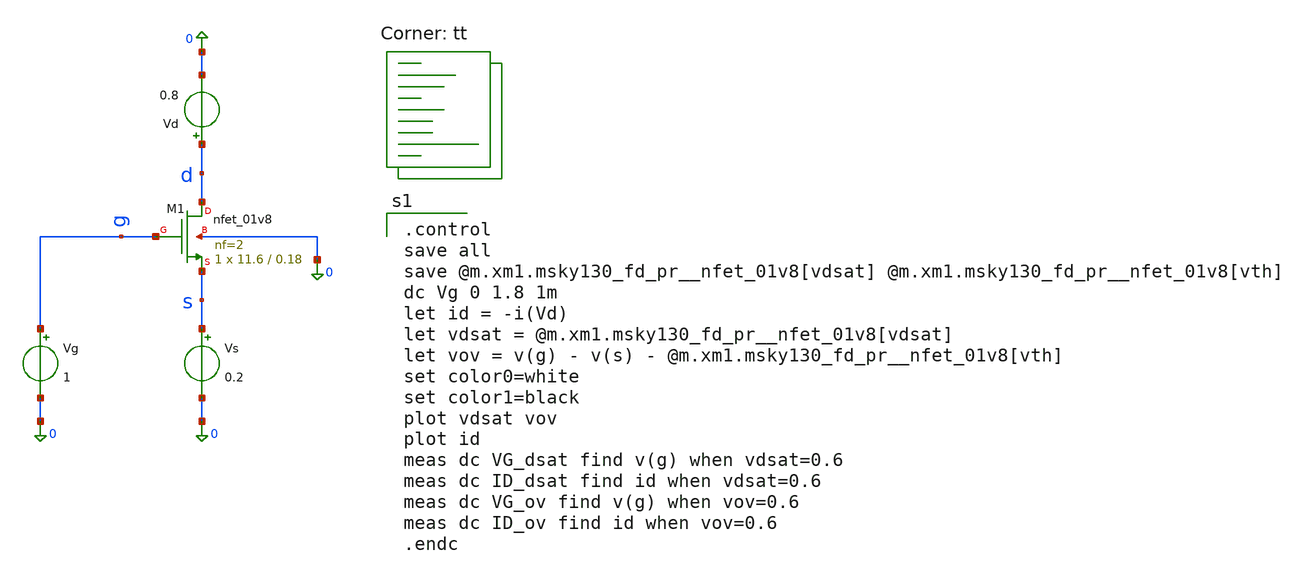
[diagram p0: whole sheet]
** sch_path: Homework 6 - Simulation on Open Source Softwares/Simulations/ex2_wmin.sch
**.subckt ex2_wmin
XM1 d g s 0 sky130_fd_pr__nfet_01v8 L=0.18 W=11.6 nf=2 ad='int((2 + 1)/2) * 11.6 / 2 * 0.29' as='int((2 + 2)/2) * 11.6 / 2 * 0.29'
+ pd='2*int((2 + 1)/2) * (11.6 / 2 + 0.29)' ps='2*int((2 + 2)/2) * (11.6 / 2 + 0.29)' nrd='0.29 / 11.6 '
+ nrs='0.29 / 11.6 ' sa=0 sb=0 sd=0 mult=1 m=1
Vs s 0 0.2
Vd d 0 0.8
Vg g 0 1
**** begin user architecture code
.lib $::SKYWATER_MODELS/sky130.lib.spice tt

.control
save all
save @m.xm1.msky130_fd_pr__nfet_01v8[vdsat] @m.xm1.msky130_fd_pr__nfet_01v8[vth]
dc Vg 0 1.8 1m
let id = -i(Vd)
let vdsat = @m.xm1.msky130_fd_pr__nfet_01v8[vdsat]
let vov = v(g) - v(s) - @m.xm1.msky130_fd_pr__nfet_01v8[vth]
set color0=white
set color1=black
plot vdsat vov
plot id
meas dc VG_dsat find v(g) when vdsat=0.6
meas dc ID_dsat find id when vdsat=0.6
meas dc VG_ov find v(g) when vov=0.6
meas dc ID_ov find id when vov=0.6
.endc

**** end user architecture code
**.ends
.end
